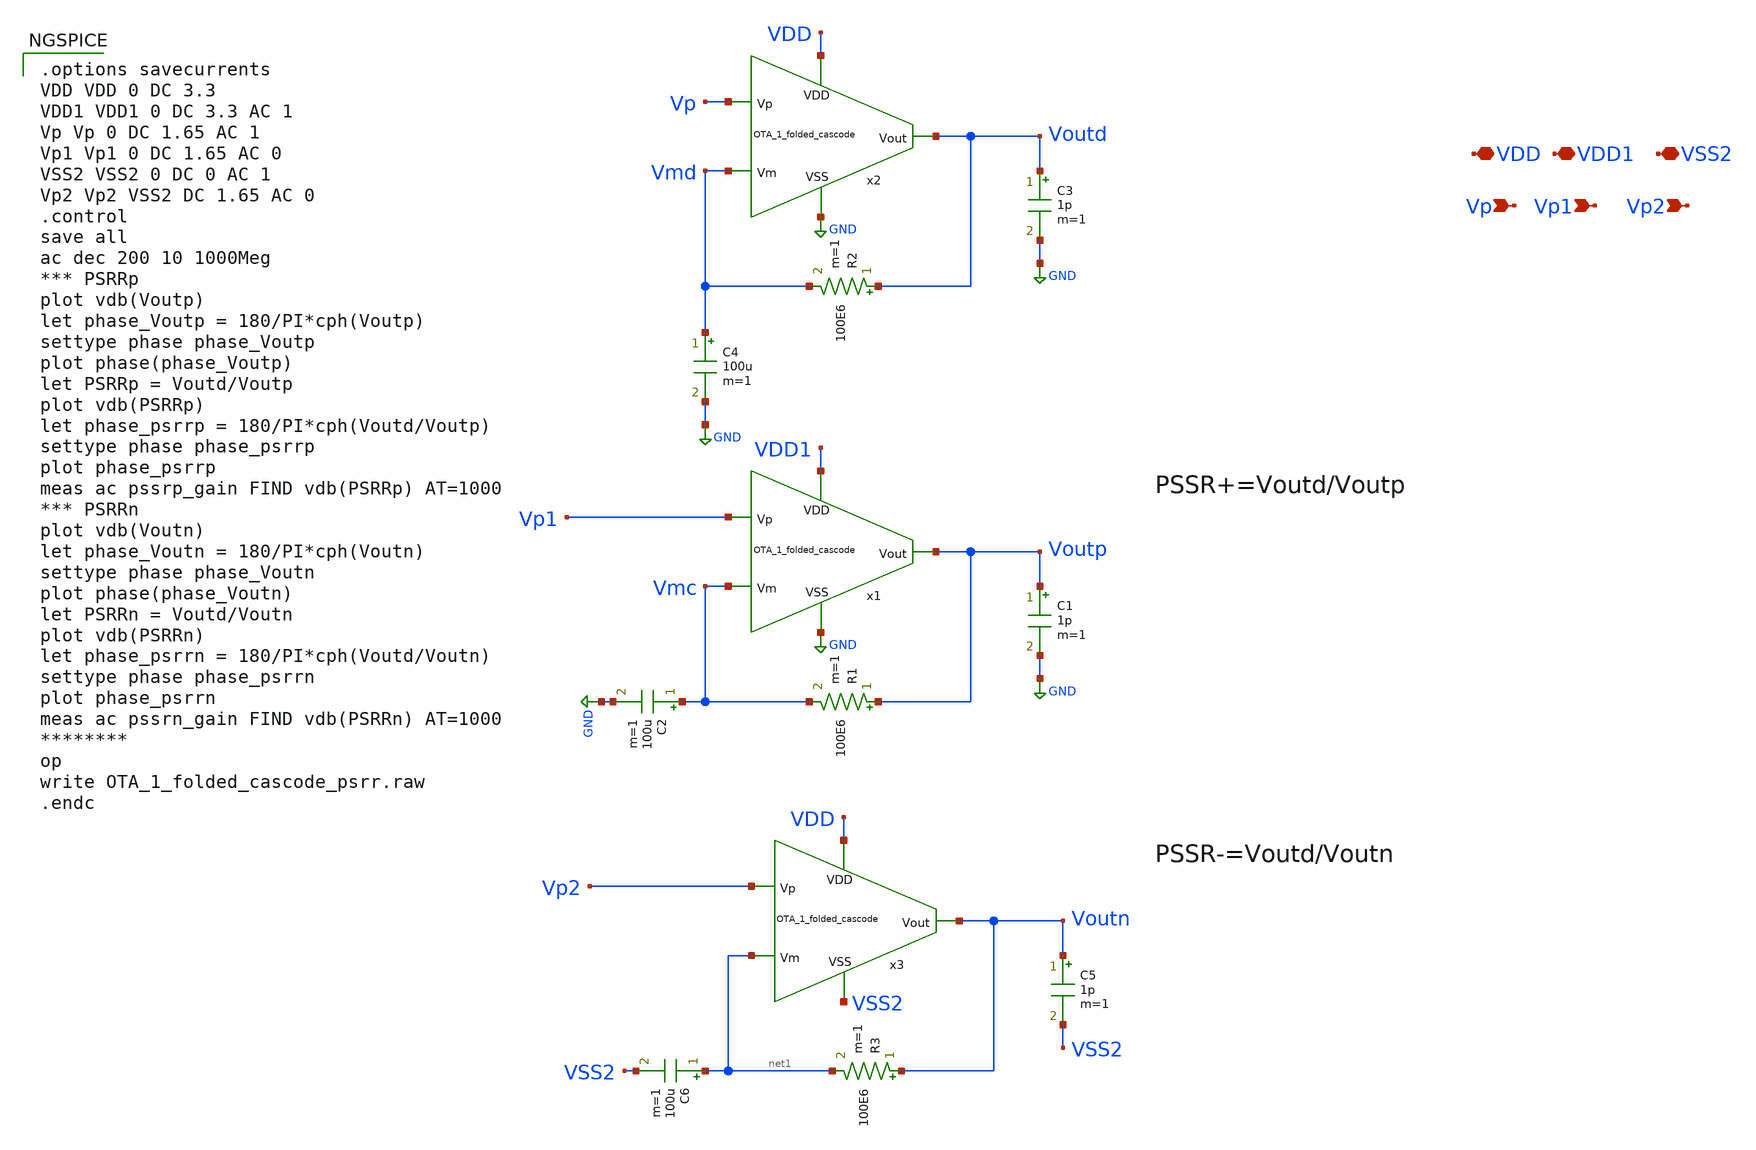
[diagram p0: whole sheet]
** sch_path: xschem/OTA_1_folded_cascode_psrr.sch
**.subckt OTA_1_folded_cascode_psrr VDD Vp VDD1 Vp1 VSS2 Vp2
*.iopin VDD
*.ipin Vp
*.iopin VDD1
*.ipin Vp1
*.iopin VSS2
*.ipin Vp2
C1 Voutp GND 1p m=1
R1 Voutp Vmc 100E6 m=1
C2 Vmc GND 100u m=1
x1 VDD1 Vp1 GND Vmc Voutp OTA_1_folded_cascode
C3 Voutd GND 1p m=1
R2 Voutd Vmd 100E6 m=1
C4 Vmd GND 100u m=1
x2 VDD Vp GND Vmd Voutd OTA_1_folded_cascode
C5 Voutn VSS2 1p m=1
R3 Voutn net1 100E6 m=1
C6 net1 VSS2 100u m=1
x3 VDD Vp2 VSS2 net1 Voutn OTA_1_folded_cascode
**** begin user architecture code

.options savecurrents
VDD VDD 0 DC 3.3
VDD1 VDD1 0 DC 3.3 AC 1
Vp Vp 0 DC 1.65 AC 1
Vp1 Vp1 0 DC 1.65 AC 0
VSS2 VSS2 0 DC 0 AC 1
Vp2 Vp2 VSS2 DC 1.65 AC 0
.control
save all
ac dec 200 10 1000Meg
*** PSRRp
plot vdb(Voutp)
let phase_Voutp = 180/PI*cph(Voutp)
settype phase phase_Voutp
plot phase(phase_Voutp)
let PSRRp = Voutd/Voutp
plot vdb(PSRRp)
let phase_psrrp = 180/PI*cph(Voutd/Voutp)
settype phase phase_psrrp
plot phase_psrrp
meas ac pssrp_gain FIND vdb(PSRRp) AT=1000
*** PSRRn
plot vdb(Voutn)
let phase_Voutn = 180/PI*cph(Voutn)
settype phase phase_Voutn
plot phase(phase_Voutn)
let PSRRn = Voutd/Voutn
plot vdb(PSRRn)
let phase_psrrn = 180/PI*cph(Voutd/Voutn)
settype phase phase_psrrn
plot phase_psrrn
meas ac pssrn_gain FIND vdb(PSRRn) AT=1000
********
op
write OTA_1_folded_cascode_psrr.raw
.endc



** opencircuitdesign pdks install
.lib $::SKYWATER_MODELS/sky130.lib.spice tt


**** end user architecture code
**.ends

* expanding   symbol:  OTA_1_folded_cascode.sym # of pins=5
** sym_path: xschem/OTA_1_folded_cascode.sym
** sch_path: xschem/OTA_1_folded_cascode.sch
.subckt OTA_1_folded_cascode VDD Vp VSS Vm Vout
*.iopin VDD
*.iopin VSS
*.ipin Vp
*.ipin Vm
*.opin Vout
XM1 Vo1 Vtop VDD VDD sky130_fd_pr__pfet_g5v0d10v5 L=1 W=5 nf=1 ad='int((nf+1)/2) * W/nf * 0.29' as='int((nf+2)/2) * W/nf * 0.29'
+ pd='2*int((nf+1)/2) * (W/nf + 0.29)' ps='2*int((nf+2)/2) * (W/nf + 0.29)' nrd='0.29 / W' nrs='0.29 / W'
+ sa=0 sb=0 sd=0 mult=5 m=5
XM7 Vo1 Vp net1 VSS sky130_fd_pr__nfet_g5v0d10v5 L=1 W=5 nf=1 ad='int((nf+1)/2) * W/nf * 0.29' as='int((nf+2)/2) * W/nf * 0.29'
+ pd='2*int((nf+1)/2) * (W/nf + 0.29)' ps='2*int((nf+2)/2) * (W/nf + 0.29)' nrd='0.29 / W' nrs='0.29 / W'
+ sa=0 sb=0 sd=0 mult=5 m=5
XM2 Vo1 Vtop VDD VDD sky130_fd_pr__pfet_g5v0d10v5 L=1 W=5 nf=1 ad='int((nf+1)/2) * W/nf * 0.29' as='int((nf+2)/2) * W/nf * 0.29'
+ pd='2*int((nf+1)/2) * (W/nf + 0.29)' ps='2*int((nf+2)/2) * (W/nf + 0.29)' nrd='0.29 / W' nrs='0.29 / W'
+ sa=0 sb=0 sd=0 mult=5 m=5
XM3 Vo2 Vtop VDD VDD sky130_fd_pr__pfet_g5v0d10v5 L=1 W=5 nf=1 ad='int((nf+1)/2) * W/nf * 0.29' as='int((nf+2)/2) * W/nf * 0.29'
+ pd='2*int((nf+1)/2) * (W/nf + 0.29)' ps='2*int((nf+2)/2) * (W/nf + 0.29)' nrd='0.29 / W' nrs='0.29 / W'
+ sa=0 sb=0 sd=0 mult=5 m=5
XM4 Vo2 Vtop VDD VDD sky130_fd_pr__pfet_g5v0d10v5 L=1 W=5 nf=1 ad='int((nf+1)/2) * W/nf * 0.29' as='int((nf+2)/2) * W/nf * 0.29'
+ pd='2*int((nf+1)/2) * (W/nf + 0.29)' ps='2*int((nf+2)/2) * (W/nf + 0.29)' nrd='0.29 / W' nrs='0.29 / W'
+ sa=0 sb=0 sd=0 mult=5 m=5
XM5 Vtop Vbias2 Vo1 VDD sky130_fd_pr__pfet_g5v0d10v5 L=1 W=5 nf=1 ad='int((nf+1)/2) * W/nf * 0.29' as='int((nf+2)/2) * W/nf * 0.29'
+ pd='2*int((nf+1)/2) * (W/nf + 0.29)' ps='2*int((nf+2)/2) * (W/nf + 0.29)' nrd='0.29 / W' nrs='0.29 / W'
+ sa=0 sb=0 sd=0 mult=5 m=5
XM6 Vout Vbias2 Vo2 VDD sky130_fd_pr__pfet_g5v0d10v5 L=1 W=5 nf=1 ad='int((nf+1)/2) * W/nf * 0.29' as='int((nf+2)/2) * W/nf * 0.29'
+ pd='2*int((nf+1)/2) * (W/nf + 0.29)' ps='2*int((nf+2)/2) * (W/nf + 0.29)' nrd='0.29 / W' nrs='0.29 / W'
+ sa=0 sb=0 sd=0 mult=5 m=5
XM8 Vo2 Vm net1 VSS sky130_fd_pr__nfet_g5v0d10v5 L=1 W=5 nf=1 ad='int((nf+1)/2) * W/nf * 0.29' as='int((nf+2)/2) * W/nf * 0.29'
+ pd='2*int((nf+1)/2) * (W/nf + 0.29)' ps='2*int((nf+2)/2) * (W/nf + 0.29)' nrd='0.29 / W' nrs='0.29 / W'
+ sa=0 sb=0 sd=0 mult=5 m=5
XM9 net1 Vbias3 net2 VSS sky130_fd_pr__nfet_g5v0d10v5 L=1 W=5 nf=1 ad='int((nf+1)/2) * W/nf * 0.29' as='int((nf+2)/2) * W/nf * 0.29'
+ pd='2*int((nf+1)/2) * (W/nf + 0.29)' ps='2*int((nf+2)/2) * (W/nf + 0.29)' nrd='0.29 / W' nrs='0.29 / W'
+ sa=0 sb=0 sd=0 mult=1.05 m=1.05
XM10 net1 Vbias3 net3 VSS sky130_fd_pr__nfet_g5v0d10v5 L=1 W=5 nf=1 ad='int((nf+1)/2) * W/nf * 0.29'
+ as='int((nf+2)/2) * W/nf * 0.29' pd='2*int((nf+1)/2) * (W/nf + 0.29)' ps='2*int((nf+2)/2) * (W/nf + 0.29)'
+ nrd='0.29 / W' nrs='0.29 / W' sa=0 sb=0 sd=0 mult=1.05 m=1.05
XM11 net2 Vbias4 VSS VSS sky130_fd_pr__nfet_g5v0d10v5 L=1 W=5 nf=1 ad='int((nf+1)/2) * W/nf * 0.29' as='int((nf+2)/2) * W/nf * 0.29'
+ pd='2*int((nf+1)/2) * (W/nf + 0.29)' ps='2*int((nf+2)/2) * (W/nf + 0.29)' nrd='0.29 / W' nrs='0.29 / W'
+ sa=0 sb=0 sd=0 mult=1.05 m=1.05
XM12 net3 Vbias4 VSS VSS sky130_fd_pr__nfet_g5v0d10v5 L=1 W=5 nf=1 ad='int((nf+1)/2) * W/nf * 0.29' as='int((nf+2)/2) * W/nf * 0.29'
+ pd='2*int((nf+1)/2) * (W/nf + 0.29)' ps='2*int((nf+2)/2) * (W/nf + 0.29)' nrd='0.29 / W' nrs='0.29 / W'
+ sa=0 sb=0 sd=0 mult=1.05 m=1.05
XM13 Vtop Vbias3 net4 VSS sky130_fd_pr__nfet_g5v0d10v5 L=1 W=5 nf=1 ad='int((nf+1)/2) * W/nf * 0.29'
+ as='int((nf+2)/2) * W/nf * 0.29' pd='2*int((nf+1)/2) * (W/nf + 0.29)' ps='2*int((nf+2)/2) * (W/nf + 0.29)'
+ nrd='0.29 / W' nrs='0.29 / W' sa=0 sb=0 sd=0 mult=1 m=1
XM14 Vout Vbias3 net5 VSS sky130_fd_pr__nfet_g5v0d10v5 L=1 W=5 nf=1 ad='int((nf+1)/2) * W/nf * 0.29'
+ as='int((nf+2)/2) * W/nf * 0.29' pd='2*int((nf+1)/2) * (W/nf + 0.29)' ps='2*int((nf+2)/2) * (W/nf + 0.29)'
+ nrd='0.29 / W' nrs='0.29 / W' sa=0 sb=0 sd=0 mult=1 m=1
XM15 net4 Vbias4 VSS VSS sky130_fd_pr__nfet_g5v0d10v5 L=1 W=5 nf=1 ad='int((nf+1)/2) * W/nf * 0.29' as='int((nf+2)/2) * W/nf * 0.29'
+ pd='2*int((nf+1)/2) * (W/nf + 0.29)' ps='2*int((nf+2)/2) * (W/nf + 0.29)' nrd='0.29 / W' nrs='0.29 / W'
+ sa=0 sb=0 sd=0 mult=1 m=1
XM16 net5 Vbias4 VSS VSS sky130_fd_pr__nfet_g5v0d10v5 L=1 W=5 nf=1 ad='int((nf+1)/2) * W/nf * 0.29' as='int((nf+2)/2) * W/nf * 0.29'
+ pd='2*int((nf+1)/2) * (W/nf + 0.29)' ps='2*int((nf+2)/2) * (W/nf + 0.29)' nrd='0.29 / W' nrs='0.29 / W'
+ sa=0 sb=0 sd=0 mult=1 m=1
x1 Vbiasp Vbiasn VSS Vbias1 Vbias2 Vbias3 Vbias4 Vlow Vhigh Vncas Vpcas VDD bias_circuit
.ends


* expanding   symbol:  bias_circuit.sym # of pins=12
** sym_path: xschem/bias_circuit.sym
** sch_path: xschem/bias_circuit.sch
.subckt bias_circuit Vbiasp Vbiasn VSS Vbias1 Vbias2 Vbias3 Vbias4 Vlow Vhigh Vncas Vpcas VDD
*.iopin VDD
*.opin Vbiasp
*.opin Vbiasn
*.iopin VSS
*.opin Vbias1
*.opin Vbias2
*.opin Vbias3
*.opin Vbias4
*.opin Vlow
*.opin Vhigh
*.opin Vncas
*.opin Vpcas
XM1 Vbias3 Vbiasp VDD VDD sky130_fd_pr__pfet_g5v0d10v5 L=1 W=5 nf=1 ad='int((nf+1)/2) * W/nf * 0.29'
+ as='int((nf+2)/2) * W/nf * 0.29' pd='2*int((nf+1)/2) * (W/nf + 0.29)' ps='2*int((nf+2)/2) * (W/nf + 0.29)'
+ nrd='0.29 / W' nrs='0.29 / W' sa=0 sb=0 sd=0 mult=5 m=5
XM3w Vbias3 Vbias3 VSS VSS sky130_fd_pr__nfet_g5v0d10v5 L=5 W=5 nf=1 ad='int((nf+1)/2) * W/nf * 0.29'
+ as='int((nf+2)/2) * W/nf * 0.29' pd='2*int((nf+1)/2) * (W/nf + 0.29)' ps='2*int((nf+2)/2) * (W/nf + 0.29)'
+ nrd='0.29 / W' nrs='0.29 / W' sa=0 sb=0 sd=0 mult=2 m=2
XM2 Vbias4 Vbiasp VDD VDD sky130_fd_pr__pfet_g5v0d10v5 L=1 W=5 nf=1 ad='int((nf+1)/2) * W/nf * 0.29'
+ as='int((nf+2)/2) * W/nf * 0.29' pd='2*int((nf+1)/2) * (W/nf + 0.29)' ps='2*int((nf+2)/2) * (W/nf + 0.29)'
+ nrd='0.29 / W' nrs='0.29 / W' sa=0 sb=0 sd=0 mult=5 m=5
XM3 Vbias4 Vbias3 Vlow VSS sky130_fd_pr__nfet_g5v0d10v5 L=1 W=5 nf=1 ad='int((nf+1)/2) * W/nf * 0.29'
+ as='int((nf+2)/2) * W/nf * 0.29' pd='2*int((nf+1)/2) * (W/nf + 0.29)' ps='2*int((nf+2)/2) * (W/nf + 0.29)'
+ nrd='0.29 / W' nrs='0.29 / W' sa=0 sb=0 sd=0 mult=1 m=1
XM4 Vlow Vbias4 VSS VSS sky130_fd_pr__nfet_g5v0d10v5 L=1 W=5 nf=1 ad='int((nf+1)/2) * W/nf * 0.29' as='int((nf+2)/2) * W/nf * 0.29'
+ pd='2*int((nf+1)/2) * (W/nf + 0.29)' ps='2*int((nf+2)/2) * (W/nf + 0.29)' nrd='0.29 / W' nrs='0.29 / W'
+ sa=0 sb=0 sd=0 mult=1 m=1
XM6 net1 Vbias2 net2 VDD sky130_fd_pr__pfet_g5v0d10v5 L=1 W=5 nf=1 ad='int((nf+1)/2) * W/nf * 0.29' as='int((nf+2)/2) * W/nf * 0.29'
+ pd='2*int((nf+1)/2) * (W/nf + 0.29)' ps='2*int((nf+2)/2) * (W/nf + 0.29)' nrd='0.29 / W' nrs='0.29 / W'
+ sa=0 sb=0 sd=0 mult=5 m=5
XM7 Vpcas Vpcas net1 VDD sky130_fd_pr__pfet_g5v0d10v5 L=1 W=5 nf=1 ad='int((nf+1)/2) * W/nf * 0.29' as='int((nf+2)/2) * W/nf * 0.29'
+ pd='2*int((nf+1)/2) * (W/nf + 0.29)' ps='2*int((nf+2)/2) * (W/nf + 0.29)' nrd='0.29 / W' nrs='0.29 / W'
+ sa=0 sb=0 sd=0 mult=5 m=5
XM5 net2 net1 VDD VDD sky130_fd_pr__pfet_g5v0d10v5 L=1 W=5 nf=1 ad='int((nf+1)/2) * W/nf * 0.29' as='int((nf+2)/2) * W/nf * 0.29'
+ pd='2*int((nf+1)/2) * (W/nf + 0.29)' ps='2*int((nf+2)/2) * (W/nf + 0.29)' nrd='0.29 / W' nrs='0.29 / W'
+ sa=0 sb=0 sd=0 mult=5 m=5
XM8 Vpcas Vbias3 net3 VSS sky130_fd_pr__nfet_g5v0d10v5 L=1 W=5 nf=1 ad='int((nf+1)/2) * W/nf * 0.29'
+ as='int((nf+2)/2) * W/nf * 0.29' pd='2*int((nf+1)/2) * (W/nf + 0.29)' ps='2*int((nf+2)/2) * (W/nf + 0.29)'
+ nrd='0.29 / W' nrs='0.29 / W' sa=0 sb=0 sd=0 mult=1 m=1
XM9 net3 Vbias4 VSS VSS sky130_fd_pr__nfet_g5v0d10v5 L=1 W=5 nf=1 ad='int((nf+1)/2) * W/nf * 0.29' as='int((nf+2)/2) * W/nf * 0.29'
+ pd='2*int((nf+1)/2) * (W/nf + 0.29)' ps='2*int((nf+2)/2) * (W/nf + 0.29)' nrd='0.29 / W' nrs='0.29 / W'
+ sa=0 sb=0 sd=0 mult=1 m=1
XM10 Vbias2 Vbias3 net4 VSS sky130_fd_pr__nfet_g5v0d10v5 L=1 W=5 nf=1 ad='int((nf+1)/2) * W/nf * 0.29'
+ as='int((nf+2)/2) * W/nf * 0.29' pd='2*int((nf+1)/2) * (W/nf + 0.29)' ps='2*int((nf+2)/2) * (W/nf + 0.29)'
+ nrd='0.29 / W' nrs='0.29 / W' sa=0 sb=0 sd=0 mult=1 m=1
XM11 net4 Vbias4 VSS VSS sky130_fd_pr__nfet_g5v0d10v5 L=1 W=5 nf=1 ad='int((nf+1)/2) * W/nf * 0.29' as='int((nf+2)/2) * W/nf * 0.29'
+ pd='2*int((nf+1)/2) * (W/nf + 0.29)' ps='2*int((nf+2)/2) * (W/nf + 0.29)' nrd='0.29 / W' nrs='0.29 / W'
+ sa=0 sb=0 sd=0 mult=1 m=1
XM12w Vbias2 Vbias2 VDD VDD sky130_fd_pr__pfet_g5v0d10v5 L=5 W=5 nf=1 ad='int((nf+1)/2) * W/nf * 0.29'
+ as='int((nf+2)/2) * W/nf * 0.29' pd='2*int((nf+1)/2) * (W/nf + 0.29)' ps='2*int((nf+2)/2) * (W/nf + 0.29)'
+ nrd='0.29 / W' nrs='0.29 / W' sa=0 sb=0 sd=0 mult=5 m=5
XM12 Vbias1 Vbias2 Vhigh VDD sky130_fd_pr__pfet_g5v0d10v5 L=1 W=5 nf=1 ad='int((nf+1)/2) * W/nf * 0.29'
+ as='int((nf+2)/2) * W/nf * 0.29' pd='2*int((nf+1)/2) * (W/nf + 0.29)' ps='2*int((nf+2)/2) * (W/nf + 0.29)'
+ nrd='0.29 / W' nrs='0.29 / W' sa=0 sb=0 sd=0 mult=5 m=5
XM13 Vhigh Vbias1 VDD VDD sky130_fd_pr__pfet_g5v0d10v5 L=1 W=5 nf=1 ad='int((nf+1)/2) * W/nf * 0.29'
+ as='int((nf+2)/2) * W/nf * 0.29' pd='2*int((nf+1)/2) * (W/nf + 0.29)' ps='2*int((nf+2)/2) * (W/nf + 0.29)'
+ nrd='0.29 / W' nrs='0.29 / W' sa=0 sb=0 sd=0 mult=5 m=5
XM14 Vbias1 Vbias3 net5 VSS sky130_fd_pr__nfet_g5v0d10v5 L=1 W=5 nf=1 ad='int((nf+1)/2) * W/nf * 0.29'
+ as='int((nf+2)/2) * W/nf * 0.29' pd='2*int((nf+1)/2) * (W/nf + 0.29)' ps='2*int((nf+2)/2) * (W/nf + 0.29)'
+ nrd='0.29 / W' nrs='0.29 / W' sa=0 sb=0 sd=0 mult=1 m=1
XM15 net5 Vbias4 VSS VSS sky130_fd_pr__nfet_g5v0d10v5 L=1 W=5 nf=1 ad='int((nf+1)/2) * W/nf * 0.29' as='int((nf+2)/2) * W/nf * 0.29'
+ pd='2*int((nf+1)/2) * (W/nf + 0.29)' ps='2*int((nf+2)/2) * (W/nf + 0.29)' nrd='0.29 / W' nrs='0.29 / W'
+ sa=0 sb=0 sd=0 mult=1 m=1
XM16 Vncas Vbias2 net6 VDD sky130_fd_pr__pfet_g5v0d10v5 L=1 W=5 nf=1 ad='int((nf+1)/2) * W/nf * 0.29'
+ as='int((nf+2)/2) * W/nf * 0.29' pd='2*int((nf+1)/2) * (W/nf + 0.29)' ps='2*int((nf+2)/2) * (W/nf + 0.29)'
+ nrd='0.29 / W' nrs='0.29 / W' sa=0 sb=0 sd=0 mult=5 m=5
XM17 net6 Vbias1 VDD VDD sky130_fd_pr__pfet_g5v0d10v5 L=1 W=5 nf=1 ad='int((nf+1)/2) * W/nf * 0.29' as='int((nf+2)/2) * W/nf * 0.29'
+ pd='2*int((nf+1)/2) * (W/nf + 0.29)' ps='2*int((nf+2)/2) * (W/nf + 0.29)' nrd='0.29 / W' nrs='0.29 / W'
+ sa=0 sb=0 sd=0 mult=5 m=5
XM18 Vncas Vncas net7 VSS sky130_fd_pr__nfet_g5v0d10v5 L=1 W=5 nf=1 ad='int((nf+1)/2) * W/nf * 0.29'
+ as='int((nf+2)/2) * W/nf * 0.29' pd='2*int((nf+1)/2) * (W/nf + 0.29)' ps='2*int((nf+2)/2) * (W/nf + 0.29)'
+ nrd='0.29 / W' nrs='0.29 / W' sa=0 sb=0 sd=0 mult=1 m=1
XM19 net7 Vbias3 net8 VSS sky130_fd_pr__nfet_g5v0d10v5 L=1 W=5 nf=1 ad='int((nf+1)/2) * W/nf * 0.29'
+ as='int((nf+2)/2) * W/nf * 0.29' pd='2*int((nf+1)/2) * (W/nf + 0.29)' ps='2*int((nf+2)/2) * (W/nf + 0.29)'
+ nrd='0.29 / W' nrs='0.29 / W' sa=0 sb=0 sd=0 mult=1 m=1
XM20 net8 net7 VSS VSS sky130_fd_pr__nfet_g5v0d10v5 L=1 W=5 nf=1 ad='int((nf+1)/2) * W/nf * 0.29' as='int((nf+2)/2) * W/nf * 0.29'
+ pd='2*int((nf+1)/2) * (W/nf + 0.29)' ps='2*int((nf+2)/2) * (W/nf + 0.29)' nrd='0.29 / W' nrs='0.29 / W'
+ sa=0 sb=0 sd=0 mult=1 m=1
x1 VDD VSS Vbiasp Vbiasn beta_multiplier
.ends


* expanding   symbol:  beta_multiplier.sym # of pins=4
** sym_path: xschem/beta_multiplier.sym
** sch_path: xschem/beta_multiplier.sch
.subckt beta_multiplier VDD VSS Vbiasp Vbiasn
*.iopin VDD
*.opin Vbiasp
*.opin Vbiasn
*.iopin VSS
XM1 net2 Vbiasp VDD VDD sky130_fd_pr__pfet_g5v0d10v5 L=1 W=5 nf=1 ad='int((nf+1)/2) * W/nf * 0.29' as='int((nf+2)/2) * W/nf * 0.29'
+ pd='2*int((nf+1)/2) * (W/nf + 0.29)' ps='2*int((nf+2)/2) * (W/nf + 0.29)' nrd='0.29 / W' nrs='0.29 / W'
+ sa=0 sb=0 sd=0 mult=5 m=5
XM3 Vbiasn Vbiasn VSS VSS sky130_fd_pr__nfet_g5v0d10v5 L=1 W=5 nf=1 ad='int((nf+1)/2) * W/nf * 0.29'
+ as='int((nf+2)/2) * W/nf * 0.29' pd='2*int((nf+1)/2) * (W/nf + 0.29)' ps='2*int((nf+2)/2) * (W/nf + 0.29)'
+ nrd='0.29 / W' nrs='0.29 / W' sa=0 sb=0 sd=0 mult=1 m=1
XM2 net3 Vbiasp VDD VDD sky130_fd_pr__pfet_g5v0d10v5 L=1 W=5 nf=1 ad='int((nf+1)/2) * W/nf * 0.29' as='int((nf+2)/2) * W/nf * 0.29'
+ pd='2*int((nf+1)/2) * (W/nf + 0.29)' ps='2*int((nf+2)/2) * (W/nf + 0.29)' nrd='0.29 / W' nrs='0.29 / W'
+ sa=0 sb=0 sd=0 mult=5 m=5
XM4 Vreg Vreg net1 VSS sky130_fd_pr__nfet_g5v0d10v5 L=1 W=5 nf=1 ad='int((nf+1)/2) * W/nf * 0.29' as='int((nf+2)/2) * W/nf * 0.29'
+ pd='2*int((nf+1)/2) * (W/nf + 0.29)' ps='2*int((nf+2)/2) * (W/nf + 0.29)' nrd='0.29 / W' nrs='0.29 / W'
+ sa=0 sb=0 sd=0 mult=12 m=12
Vref1 net2 Vbiasn 0
Vref2 net3 Vreg 0
XR2 VSS net1 VSS sky130_fd_pr__res_xhigh_po W=0.35 L=0.74 mult=1 m=1
XM5 net4 net4 VDD VDD sky130_fd_pr__pfet_g5v0d10v5 L=1 W=5 nf=1 ad='int((nf+1)/2) * W/nf * 0.29' as='int((nf+2)/2) * W/nf * 0.29'
+ pd='2*int((nf+1)/2) * (W/nf + 0.29)' ps='2*int((nf+2)/2) * (W/nf + 0.29)' nrd='0.29 / W' nrs='0.29 / W'
+ sa=0 sb=0 sd=0 mult=5 m=5
XM6 Vbiasp net4 VDD VDD sky130_fd_pr__pfet_g5v0d10v5 L=1 W=5 nf=1 ad='int((nf+1)/2) * W/nf * 0.29' as='int((nf+2)/2) * W/nf * 0.29'
+ pd='2*int((nf+1)/2) * (W/nf + 0.29)' ps='2*int((nf+2)/2) * (W/nf + 0.29)' nrd='0.29 / W' nrs='0.29 / W'
+ sa=0 sb=0 sd=0 mult=5 m=5
XM7 net4 Vreg VSS VSS sky130_fd_pr__nfet_g5v0d10v5 L=1 W=5 nf=1 ad='int((nf+1)/2) * W/nf * 0.29' as='int((nf+2)/2) * W/nf * 0.29'
+ pd='2*int((nf+1)/2) * (W/nf + 0.29)' ps='2*int((nf+2)/2) * (W/nf + 0.29)' nrd='0.29 / W' nrs='0.29 / W'
+ sa=0 sb=0 sd=0 mult=1 m=1
XM8 Vbiasp Vbiasn VSS VSS sky130_fd_pr__nfet_g5v0d10v5 L=1 W=5 nf=1 ad='int((nf+1)/2) * W/nf * 0.29'
+ as='int((nf+2)/2) * W/nf * 0.29' pd='2*int((nf+1)/2) * (W/nf + 0.29)' ps='2*int((nf+2)/2) * (W/nf + 0.29)'
+ nrd='0.29 / W' nrs='0.29 / W' sa=0 sb=0 sd=0 mult=1 m=1
XM9 net5 net5 VDD VDD sky130_fd_pr__pfet_g5v0d10v5 L=40 W=1 nf=1 ad='int((nf+1)/2) * W/nf * 0.29' as='int((nf+2)/2) * W/nf * 0.29'
+ pd='2*int((nf+1)/2) * (W/nf + 0.29)' ps='2*int((nf+2)/2) * (W/nf + 0.29)' nrd='0.29 / W' nrs='0.29 / W'
+ sa=0 sb=0 sd=0 mult=1 m=1
XM10 net5 Vbiasn VSS VSS sky130_fd_pr__nfet_g5v0d10v5 L=1 W=5 nf=1 ad='int((nf+1)/2) * W/nf * 0.29' as='int((nf+2)/2) * W/nf * 0.29'
+ pd='2*int((nf+1)/2) * (W/nf + 0.29)' ps='2*int((nf+2)/2) * (W/nf + 0.29)' nrd='0.29 / W' nrs='0.29 / W'
+ sa=0 sb=0 sd=0 mult=1 m=1
XM11 Vbiasp net5 Vbiasn VSS sky130_fd_pr__nfet_g5v0d10v5 L=2 W=5 nf=1 ad='int((nf+1)/2) * W/nf * 0.29'
+ as='int((nf+2)/2) * W/nf * 0.29' pd='2*int((nf+1)/2) * (W/nf + 0.29)' ps='2*int((nf+2)/2) * (W/nf + 0.29)'
+ nrd='0.29 / W' nrs='0.29 / W' sa=0 sb=0 sd=0 mult=1 m=1
XM12 VDD Vbiasp VDD VDD sky130_fd_pr__pfet_g5v0d10v5 L=25 W=5 nf=1 ad='int((nf+1)/2) * W/nf * 0.29' as='int((nf+2)/2) * W/nf * 0.29'
+ pd='2*int((nf+1)/2) * (W/nf + 0.29)' ps='2*int((nf+2)/2) * (W/nf + 0.29)' nrd='0.29 / W' nrs='0.29 / W'
+ sa=0 sb=0 sd=0 mult=5 m=5
.ends

.GLOBAL GND
.end
